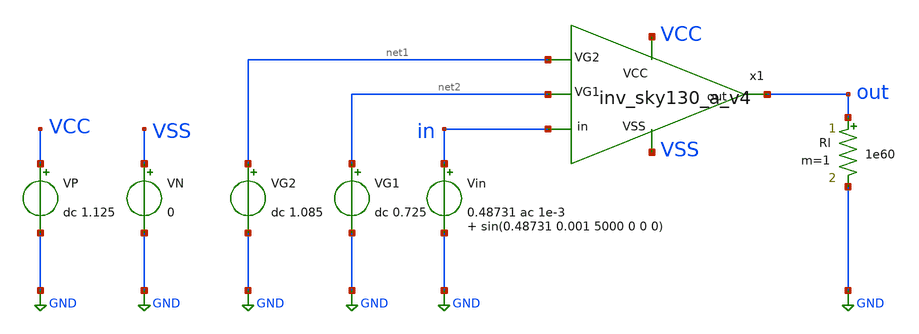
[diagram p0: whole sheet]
** sch_path: Amplifier_Inv/xschem/pl/tb_inv_sky130_a_pl.sch
**.subckt tb_inv_sky130_a_pl
VN VSS GND 0
VP VCC GND dc 1.125
.save i(vp)
Vin in GND 0.48731 ac 1e-3 sin(0.48731 0.001 5000 0 0 0)
.save i(vin)
Rl out GND 1e60 m=1
VG2 net1 GND dc 1.085
VG1 net2 GND dc 0.725
x1 net2 VCC net1 out in VSS inv_sky130_a_v4
**** begin user architecture code

** opencircuitdesign pdks install
.lib $::SKYWATER_MODELS/sky130.lib.spice tt



.include /Users/miguelcorrea/Desktop/MA2_project/Amplifier_Inv/netlist/inv_sky130_a_v4_pl.spice
.control

  noise v(out) Vin dec 1000 300 10k
  save all
  setplot noise1
  write tb_inv_sky130_a_noise_spectrum_pl.raw

  noise v(out) Vin dec 1000 300 10k 10
  save all
  write tb_inv_sky130_a_noise_pl.raw

  dc Vin 0 1.125 0.00001
  save all v(out)
  write tb_inv_sky130_a_DC_pl.raw v(out)

  tran 0.1u 4m
  save all
  let pw_in = i(Vin)*v(in)
  let pw_vcc = i(Vp)*1.125
  let pw_vg1 = i(Vg1)*0.725
  let pw_vg2 = i(Vg2)*1.085
  let pw_total = pw_in+pw_vcc
  meas tran avg_pw_total AVG pw_total FROM=0 TO=2m
  meas tran avg_pw_in AVG pw_in FROM=0 TO=2m
  meas tran avg_pw_vcc AVG pw_vcc FROM=0 TO=2m
  write tb_inv_sky130_a_tran_pl.raw v(in) v(out) avg_pw_total

  ac dec 1000 1 1e8
  save all v(out) v(in)
  let gain = db(v(out)/v(in))
  let phase = phase(v(out)/v(in))
  write tb_inv_sky130_a_AC_pl.raw gain
.endc

**** end user architecture code
**.ends
.GLOBAL GND
.end
